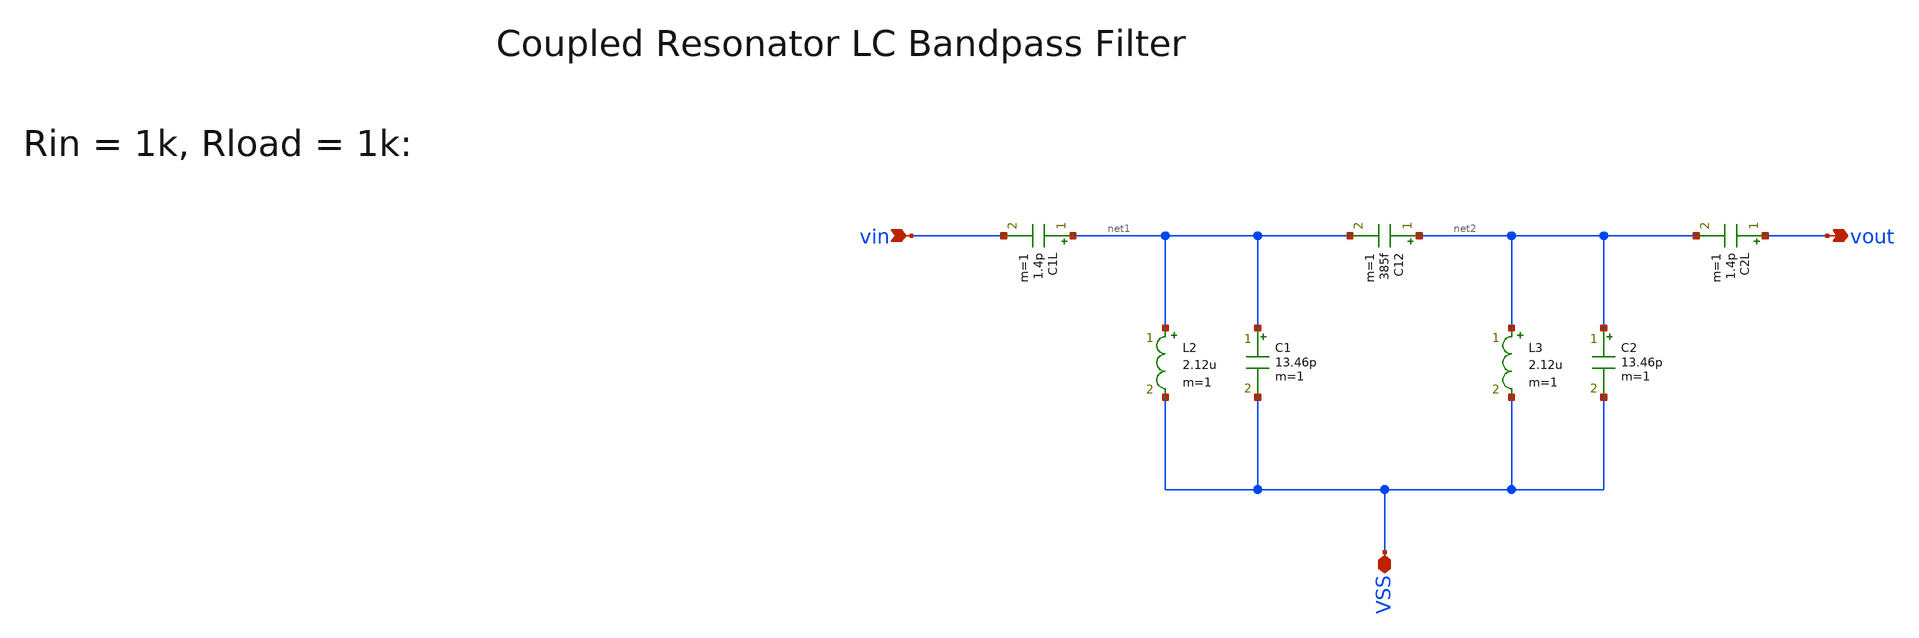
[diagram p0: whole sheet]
** sch_path: ihp130/macros/coupled_resonator_lc_bpf/schematic/coupled_resonator_lc_bpf_1k_1k.sch
**.subckt coupled_resonator_lc_bpf_1k_1k vin vout VSS
*.ipin vin
*.opin vout
*.iopin VSS
C1 net1 VSS 13.46p m=1
L2 net1 VSS 2.12u m=1
C12 net2 net1 385f m=1
C2 net2 VSS 13.46p m=1
L3 net2 VSS 2.12u m=1
C1L net1 vin 1.4p m=1
C2L vout net2 1.4p m=1
**.ends
.end
